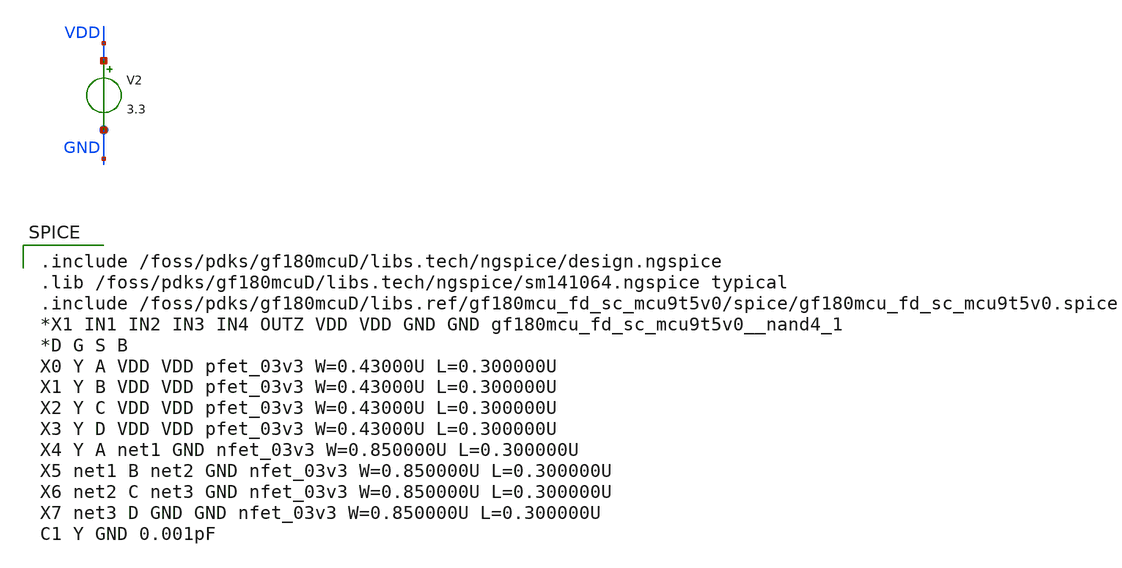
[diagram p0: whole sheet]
** sch_path: designs/libs/tb_NAND4/nand4_test.sch
**.subckt nand4_test
V2 VDD GND 3.3
**** begin user architecture code

.include /foss/pdks/gf180mcuD/libs.tech/ngspice/design.ngspice
.lib /foss/pdks/gf180mcuD/libs.tech/ngspice/sm141064.ngspice typical
.include /foss/pdks/gf180mcuD/libs.ref/gf180mcu_fd_sc_mcu9t5v0/spice/gf180mcu_fd_sc_mcu9t5v0.spice
*X1 IN1 IN2 IN3 IN4 OUTZ VDD VDD GND GND gf180mcu_fd_sc_mcu9t5v0__nand4_1
*D G S B
X0 Y A VDD VDD pfet_03v3 W=0.43000U L=0.300000U
X1 Y B VDD VDD pfet_03v3 W=0.43000U L=0.300000U
X2 Y C VDD VDD pfet_03v3 W=0.43000U L=0.300000U
X3 Y D VDD VDD pfet_03v3 W=0.43000U L=0.300000U
X4 Y A net1 GND nfet_03v3 W=0.850000U L=0.300000U
X5 net1 B net2 GND nfet_03v3 W=0.850000U L=0.300000U
X6 net2 C net3 GND nfet_03v3 W=0.850000U L=0.300000U
X7 net3 D GND GND nfet_03v3 W=0.850000U L=0.300000U
C1 Y GND 0.001pF






Vin1 A 0 PULSE(0 3.3 1n 10p 10p 10n 20n)
Vin2 B 0 DC 3.3
*Vin2 B 0 PULSE(0 3.3 2n 10p 10p 10n 20n)
Vin3 C 0 DC 3.3
*Vin3 C 0 PULSE(0 3.3 3n 10p 10p 10n 20n)
Vin4 D 0 DC 3.3
*Vin4 D 0 PULSE(0 3.3 4n 10p 10p 10n 20n)
*.tran 10p 50n
.save all

.control
tran 1p 50n
meas tran rise_result TRIG v(Y) VAL=0.33 RISE=1 TARG v(Y) VAL=2.97 RISE=1
meas tran tfall_result TRIG v(Y) VAL=2.97 FALL=1 TARG v(Y) VAL=0.33 FALL=1
meas tran tplh_A TRIG v(A) VAL=1.65 RISE=1 TARG v(Y) VAL=1.65 FALL=1
meas tran tphl_A TRIG v(A) VAL=1.65 FALL=1 TARG v(Y) VAL=1.65 RISE=1
print 0.5*(tphl_A + tplh_A)
*echo 'The tplh value for A NAND2_1 is: $&tplh_A' > /foss/designs/NAND4/schematic/NAND2_1_propagation.txt
*echo 'The tphl value for A NAND2_1 is: $&tphl_A' >> /foss/designs/NAND4/schematic/NAND2_1_propagation.txt
.endc



**** end user architecture code
**.ends
.end
